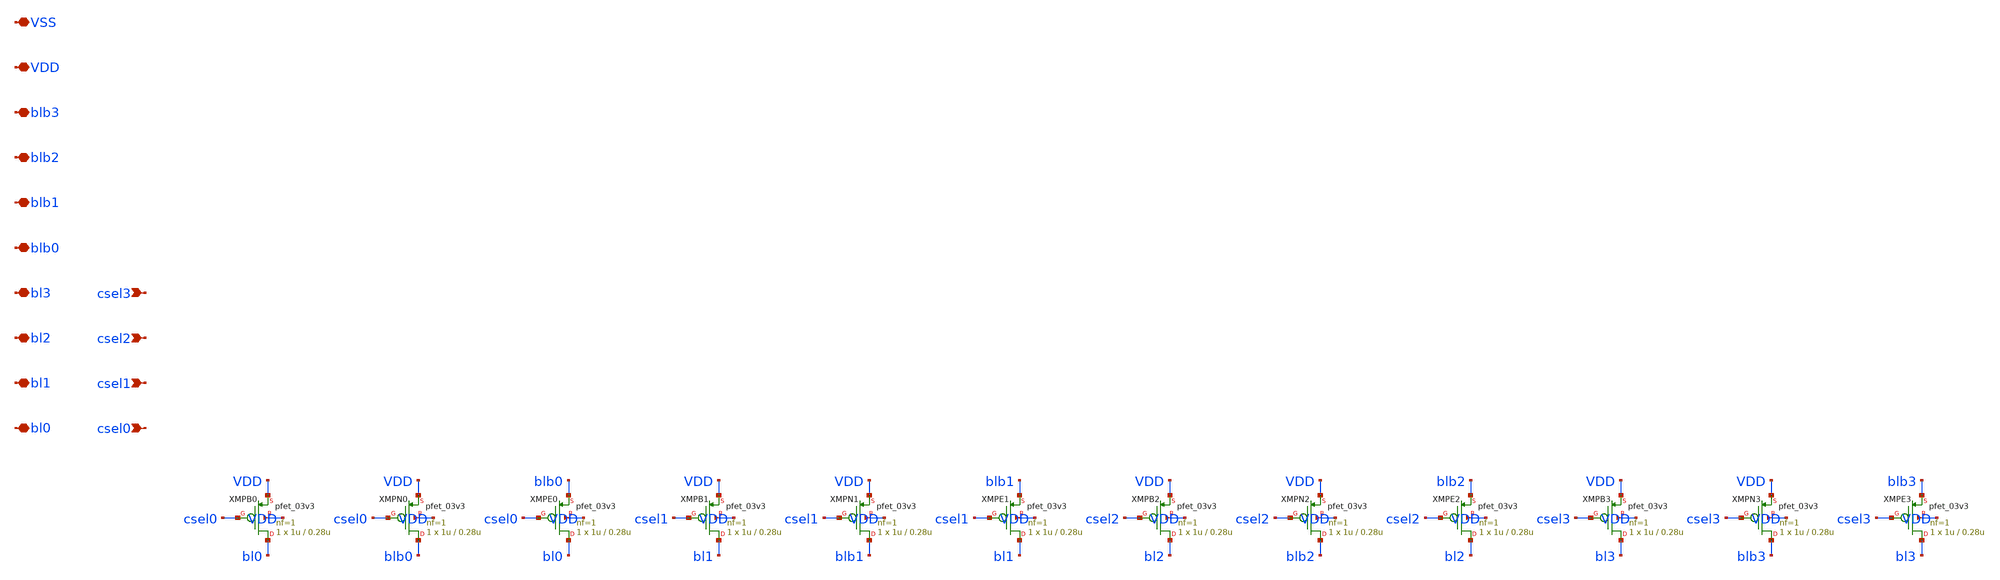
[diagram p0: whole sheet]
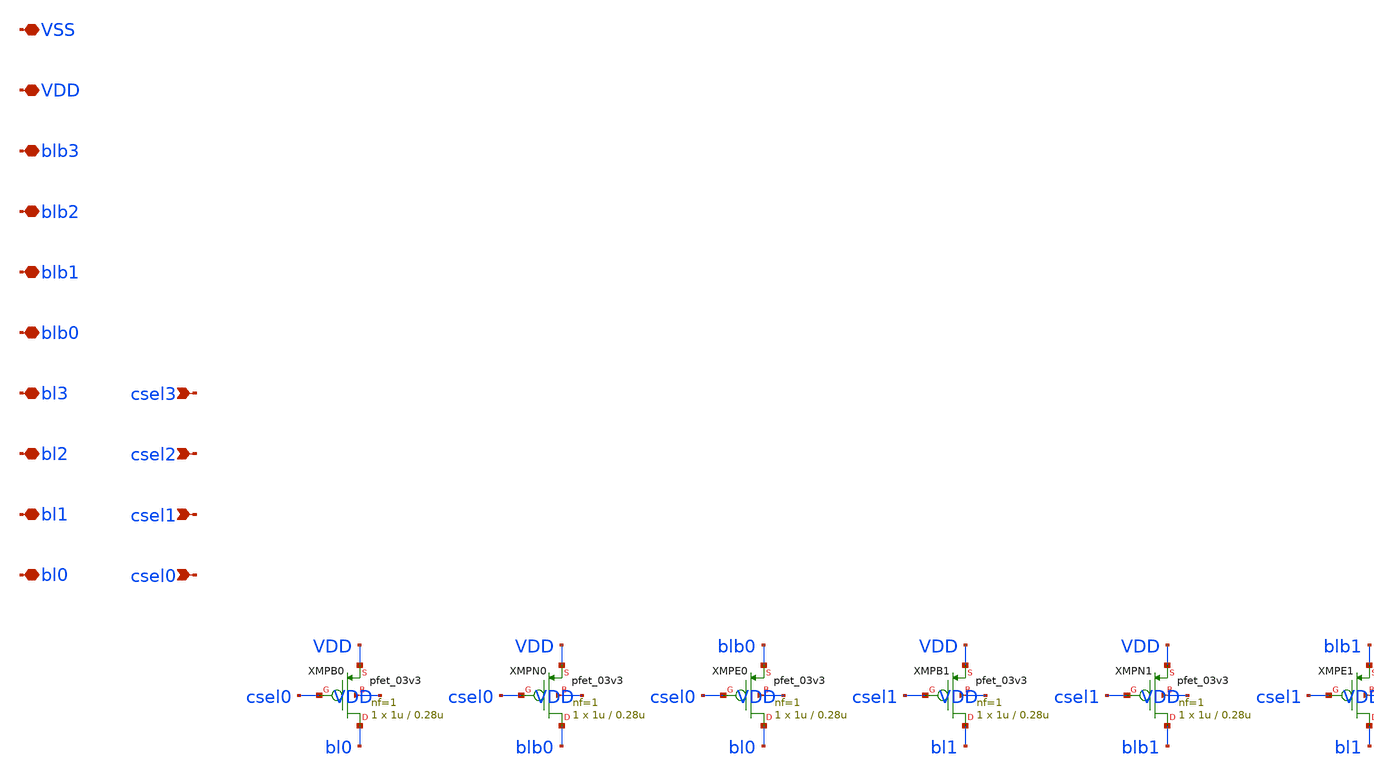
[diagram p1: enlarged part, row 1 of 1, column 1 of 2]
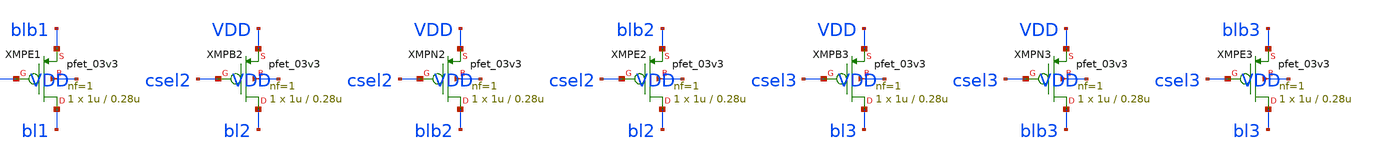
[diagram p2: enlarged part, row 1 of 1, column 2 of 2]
** sch_path: design/precharge_slice.sch
**.subckt precharge_slice csel0 csel1 csel2 csel3 bl0 bl1 bl2 bl3 blb0 blb1 blb2 blb3 VDD VSS
*.ipin csel0
*.ipin csel1
*.ipin csel2
*.ipin csel3
*.iopin bl0
*.iopin bl1
*.iopin bl2
*.iopin bl3
*.iopin blb0
*.iopin blb1
*.iopin blb2
*.iopin blb3
*.iopin VDD
*.iopin VSS
XMPB0 bl0 csel0 VDD VDD pfet_03v3 L=0.28u W=1u nf=1 ad='int((nf+1)/2) * W/nf * 0.18u' as='int((nf+2)/2) * W/nf * 0.18u'
+ pd='2*int((nf+1)/2) * (W/nf + 0.18u)' ps='2*int((nf+2)/2) * (W/nf + 0.18u)' nrd='0.18u / W' nrs='0.18u / W'
+ sa=0 sb=0 sd=0 m=1
XMPN0 blb0 csel0 VDD VDD pfet_03v3 L=0.28u W=1u nf=1 ad='int((nf+1)/2) * W/nf * 0.18u' as='int((nf+2)/2) * W/nf * 0.18u'
+ pd='2*int((nf+1)/2) * (W/nf + 0.18u)' ps='2*int((nf+2)/2) * (W/nf + 0.18u)' nrd='0.18u / W' nrs='0.18u / W'
+ sa=0 sb=0 sd=0 m=1
XMPE0 bl0 csel0 blb0 VDD pfet_03v3 L=0.28u W=1u nf=1 ad='int((nf+1)/2) * W/nf * 0.18u' as='int((nf+2)/2) * W/nf * 0.18u'
+ pd='2*int((nf+1)/2) * (W/nf + 0.18u)' ps='2*int((nf+2)/2) * (W/nf + 0.18u)' nrd='0.18u / W' nrs='0.18u / W'
+ sa=0 sb=0 sd=0 m=1
XMPB1 bl1 csel1 VDD VDD pfet_03v3 L=0.28u W=1u nf=1 ad='int((nf+1)/2) * W/nf * 0.18u' as='int((nf+2)/2) * W/nf * 0.18u'
+ pd='2*int((nf+1)/2) * (W/nf + 0.18u)' ps='2*int((nf+2)/2) * (W/nf + 0.18u)' nrd='0.18u / W' nrs='0.18u / W'
+ sa=0 sb=0 sd=0 m=1
XMPN1 blb1 csel1 VDD VDD pfet_03v3 L=0.28u W=1u nf=1 ad='int((nf+1)/2) * W/nf * 0.18u' as='int((nf+2)/2) * W/nf * 0.18u'
+ pd='2*int((nf+1)/2) * (W/nf + 0.18u)' ps='2*int((nf+2)/2) * (W/nf + 0.18u)' nrd='0.18u / W' nrs='0.18u / W'
+ sa=0 sb=0 sd=0 m=1
XMPE1 bl1 csel1 blb1 VDD pfet_03v3 L=0.28u W=1u nf=1 ad='int((nf+1)/2) * W/nf * 0.18u' as='int((nf+2)/2) * W/nf * 0.18u'
+ pd='2*int((nf+1)/2) * (W/nf + 0.18u)' ps='2*int((nf+2)/2) * (W/nf + 0.18u)' nrd='0.18u / W' nrs='0.18u / W'
+ sa=0 sb=0 sd=0 m=1
XMPB2 bl2 csel2 VDD VDD pfet_03v3 L=0.28u W=1u nf=1 ad='int((nf+1)/2) * W/nf * 0.18u' as='int((nf+2)/2) * W/nf * 0.18u'
+ pd='2*int((nf+1)/2) * (W/nf + 0.18u)' ps='2*int((nf+2)/2) * (W/nf + 0.18u)' nrd='0.18u / W' nrs='0.18u / W'
+ sa=0 sb=0 sd=0 m=1
XMPN2 blb2 csel2 VDD VDD pfet_03v3 L=0.28u W=1u nf=1 ad='int((nf+1)/2) * W/nf * 0.18u' as='int((nf+2)/2) * W/nf * 0.18u'
+ pd='2*int((nf+1)/2) * (W/nf + 0.18u)' ps='2*int((nf+2)/2) * (W/nf + 0.18u)' nrd='0.18u / W' nrs='0.18u / W'
+ sa=0 sb=0 sd=0 m=1
XMPE2 bl2 csel2 blb2 VDD pfet_03v3 L=0.28u W=1u nf=1 ad='int((nf+1)/2) * W/nf * 0.18u' as='int((nf+2)/2) * W/nf * 0.18u'
+ pd='2*int((nf+1)/2) * (W/nf + 0.18u)' ps='2*int((nf+2)/2) * (W/nf + 0.18u)' nrd='0.18u / W' nrs='0.18u / W'
+ sa=0 sb=0 sd=0 m=1
XMPB3 bl3 csel3 VDD VDD pfet_03v3 L=0.28u W=1u nf=1 ad='int((nf+1)/2) * W/nf * 0.18u' as='int((nf+2)/2) * W/nf * 0.18u'
+ pd='2*int((nf+1)/2) * (W/nf + 0.18u)' ps='2*int((nf+2)/2) * (W/nf + 0.18u)' nrd='0.18u / W' nrs='0.18u / W'
+ sa=0 sb=0 sd=0 m=1
XMPN3 blb3 csel3 VDD VDD pfet_03v3 L=0.28u W=1u nf=1 ad='int((nf+1)/2) * W/nf * 0.18u' as='int((nf+2)/2) * W/nf * 0.18u'
+ pd='2*int((nf+1)/2) * (W/nf + 0.18u)' ps='2*int((nf+2)/2) * (W/nf + 0.18u)' nrd='0.18u / W' nrs='0.18u / W'
+ sa=0 sb=0 sd=0 m=1
XMPE3 bl3 csel3 blb3 VDD pfet_03v3 L=0.28u W=1u nf=1 ad='int((nf+1)/2) * W/nf * 0.18u' as='int((nf+2)/2) * W/nf * 0.18u'
+ pd='2*int((nf+1)/2) * (W/nf + 0.18u)' ps='2*int((nf+2)/2) * (W/nf + 0.18u)' nrd='0.18u / W' nrs='0.18u / W'
+ sa=0 sb=0 sd=0 m=1
**.ends
.end
